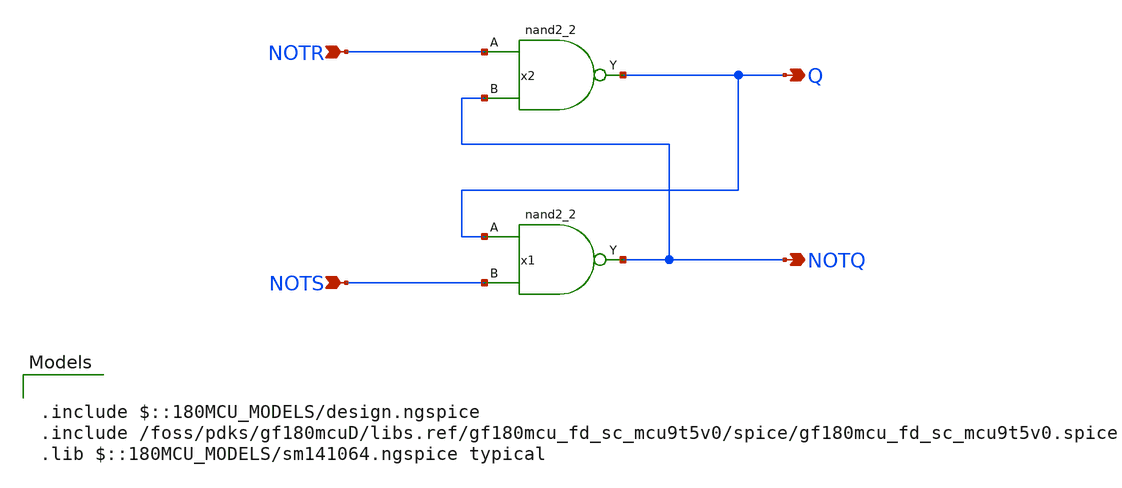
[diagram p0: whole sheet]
** sch_path: designs/switch_matrix_gf180mcu_9t5v0-main/designs/libs/core_analog/oscillator/sr_latch.sch
**.subckt sr_latch NOTR NOTS Q NOTQ
*.ipin NOTR
*.ipin NOTS
*.opin Q
*.opin NOTQ
x2 NOTR NOTQ VSSd VDDd VSSd VDDd Q gf180mcu_fd_sc_mcu9t5v0__nand2_2
x1 Q NOTS VSSd VDDd VSSd VDDd NOTQ gf180mcu_fd_sc_mcu9t5v0__nand2_2
**** begin user architecture code

.include $::180MCU_MODELS/design.ngspice
.include /foss/pdks/gf180mcuD/libs.ref/gf180mcu_fd_sc_mcu9t5v0/spice/gf180mcu_fd_sc_mcu9t5v0.spice
.lib $::180MCU_MODELS/sm141064.ngspice typical

**** end user architecture code
**.ends
.end
